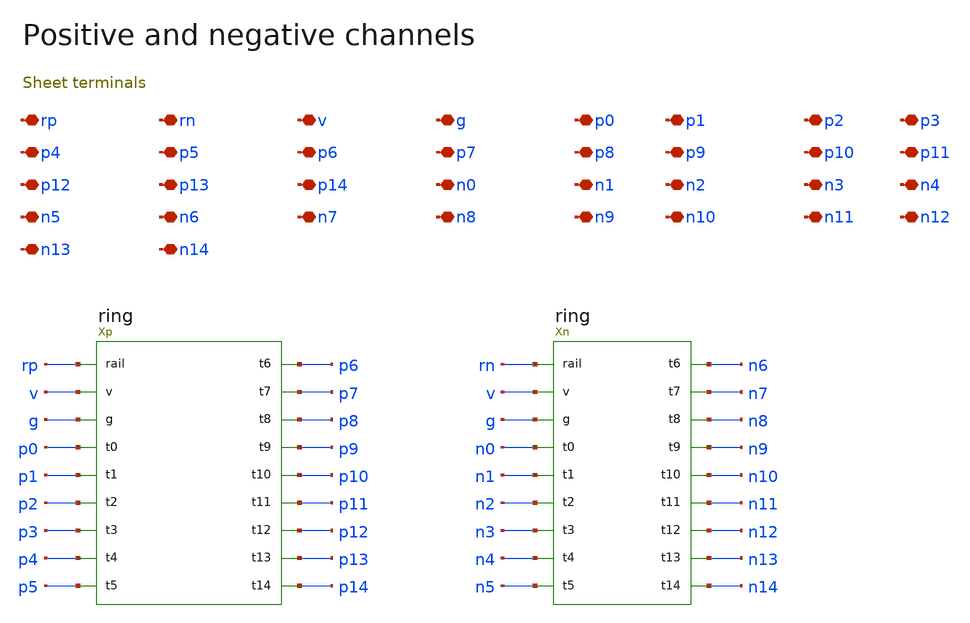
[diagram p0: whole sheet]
** sch_path: review/xschem/dual.sch
**.subckt dual rp rn v g p0 p1 p2 p3 p4 p5 p6 p7 p8 p9 p10 p11 p12 p13 p14 n0 n1 n2 n3 n4 n5 n6 n7
*+ n8 n9 n10 n11 n12 n13 n14
*.iopin rp
*.iopin rn
*.iopin v
*.iopin g
*.iopin p0
*.iopin p1
*.iopin p2
*.iopin p3
*.iopin p4
*.iopin p5
*.iopin p6
*.iopin p7
*.iopin p8
*.iopin p9
*.iopin p10
*.iopin p11
*.iopin p12
*.iopin p13
*.iopin p14
*.iopin n0
*.iopin n1
*.iopin n2
*.iopin n3
*.iopin n4
*.iopin n5
*.iopin n6
*.iopin n7
*.iopin n8
*.iopin n9
*.iopin n10
*.iopin n11
*.iopin n12
*.iopin n13
*.iopin n14
Xp rp v g p0 p1 p2 p3 p4 p5 p6 p7 p8 p9 p10 p11 p12 p13 p14 ring
Xn rn v g n0 n1 n2 n3 n4 n5 n6 n7 n8 n9 n10 n11 n12 n13 n14 ring
**.ends

* expanding   symbol:  ring.sym # of pins=18
** sym_path: review/xschem/ring.sym
** sch_path: review/xschem/ring.sch
.subckt ring rail v g t0 t1 t2 t3 t4 t5 t6 t7 t8 t9 t10 t11 t12 t13 t14
*.iopin rail
*.iopin v
*.iopin g
*.iopin t0
*.iopin t1
*.iopin t2
*.iopin t3
*.iopin t4
*.iopin t5
*.iopin t6
*.iopin t7
*.iopin t8
*.iopin t9
*.iopin t10
*.iopin t11
*.iopin t12
*.iopin t13
*.iopin t14
Xbank rail v g oa0 ob0 oa1 ob1 oa2 ob2 oa3 ob3 oa4 ob4 oa5 ob5 oa6 ob6 oa7 ob7 oa8 ob8 oa9 ob9 oa10
+ ob10 oa11 ob11 oa12 ob12 oa13 ob13 oa14 ob14 bank
Xl0 oa0 ob0 t0 v g cvsl
Xl1 oa1 ob1 t1 v g cvsl
Xl2 oa2 ob2 t2 v g cvsl
Xl3 oa3 ob3 t3 v g cvsl
Xl4 oa4 ob4 t4 v g cvsl
Xl5 oa5 ob5 t5 v g cvsl
Xl6 oa6 ob6 t6 v g cvsl
Xl7 oa7 ob7 t7 v g cvsl
Xl8 oa8 ob8 t8 v g cvsl
Xl9 oa9 ob9 t9 v g cvsl
Xl10 oa10 ob10 t10 v g cvsl
Xl11 oa11 ob11 t11 v g cvsl
Xl12 oa12 ob12 t12 v g cvsl
Xl13 oa13 ob13 t13 v g cvsl
Xl14 oa14 ob14 t14 v g cvsl
.ends


* expanding   symbol:  bank.sym # of pins=33
** sym_path: review/xschem/bank.sym
** sch_path: review/xschem/bank.sch
.subckt bank rail well g oa0 ob0 oa1 ob1 oa2 ob2 oa3 ob3 oa4 ob4 oa5 ob5 oa6 ob6 oa7 ob7 oa8 ob8 oa9
+ ob9 oa10 ob10 oa11 ob11 oa12 ob12 oa13 ob13 oa14 ob14
*.iopin rail
*.iopin well
*.iopin g
*.iopin oa0
*.iopin ob0
*.iopin oa1
*.iopin ob1
*.iopin oa2
*.iopin ob2
*.iopin oa3
*.iopin ob3
*.iopin oa4
*.iopin ob4
*.iopin oa5
*.iopin ob5
*.iopin oa6
*.iopin ob6
*.iopin oa7
*.iopin ob7
*.iopin oa8
*.iopin ob8
*.iopin oa9
*.iopin ob9
*.iopin oa10
*.iopin ob10
*.iopin oa11
*.iopin ob11
*.iopin oa12
*.iopin ob12
*.iopin oa13
*.iopin ob13
*.iopin oa14
*.iopin ob14
X0 oa14 ob14 oa0 ob0 rail g well stage
X1 oa0 ob0 oa1 ob1 rail g well stage
X2 oa1 ob1 oa2 ob2 rail g well stage
X3 oa2 ob2 oa3 ob3 rail g well stage
X4 oa3 ob3 oa4 ob4 rail g well stage
X5 oa4 ob4 oa5 ob5 rail g well stage
X6 oa5 ob5 oa6 ob6 rail g well stage
X7 oa6 ob6 oa7 ob7 rail g well stage
X8 oa7 ob7 oa8 ob8 rail g well stage
X9 oa8 ob8 oa9 ob9 rail g well stage
X10 oa9 ob9 oa10 ob10 rail g well stage
X11 oa10 ob10 oa11 ob11 rail g well stage
X12 oa11 ob11 oa12 ob12 rail g well stage
X13 oa12 ob12 oa13 ob13 rail g well stage
X14 oa13 ob13 oa14 ob14 rail g well stage
Xdummy well well dy dz g g well stage
.ends


* expanding   symbol:  cvsl.sym # of pins=5
** sym_path: review/xschem/cvsl.sym
** sch_path: review/xschem/cvsl.sch
.subckt cvsl a b out v g
*.iopin a
*.iopin b
*.iopin out
*.iopin v
*.iopin g
XMn0 l a g g sky130_fd_pr__nfet_01v8_lvt L=.15 W=4 nf=1 ad=1.16 as=1.16 pd=8.58 ps=8.58 nrd='0.29 / 4 '
+ nrs='0.29 / 4 ' sa=0 sb=0 sd=0 mult=1 m=1
XMn1 r b g g sky130_fd_pr__nfet_01v8_lvt L=.15 W=4 nf=1 ad=1.16 as=1.16 pd=8.58 ps=8.58 nrd='0.29 / 4 '
+ nrs='0.29 / 4 ' sa=0 sb=0 sd=0 mult=1 m=1
XMp0 l r v v sky130_fd_pr__pfet_01v8 L=2.4 W=.42 nf=1 ad=.122 as=.122 pd=1.42 ps=1.42 nrd='0.29 / W'
+ nrs='0.29 / W' sa=0 sb=0 sd=0 mult=1 m=1
XMp1 r l v v sky130_fd_pr__pfet_01v8 L=2.4 W=.42 nf=1 ad=.122 as=.122 pd=1.42 ps=1.42 nrd='0.29 / W'
+ nrs='0.29 / W' sa=0 sb=0 sd=0 mult=1 m=1
XMbuf_p out l v v sky130_fd_pr__pfet_01v8 L=.15 W=.84 nf=1 ad='int((nf+1)/2) * W/nf * 0.29' as='int((nf+2)/2) * W/nf * 0.29'
+ pd='2*int((nf+1)/2) * (W/nf + 0.29)' ps='2*int((nf+2)/2) * (W/nf + 0.29)' nrd='0.29 / W' nrs='0.29 / W'
+ sa=0 sb=0 sd=0 mult=1 m=1
XMbuf_n out l g g sky130_fd_pr__nfet_01v8 L=.15 W=.42 nf=1 ad='int((1 + 1)/2) * .42 / 1 * 0.29' as='int((1 + 2)/2) * .42 / 1 * 0.29'
+ pd='2*int((1 + 1)/2) * (.42 / 1 + 0.29)' ps='2*int((1 + 2)/2) * (.42 / 1 + 0.29)' nrd='0.29 / .42 ' nrs='0.29 / .42 '
+ sa=0 sb=0 sd=0 mult=1 m=1
XMdummy_p dummy r v v sky130_fd_pr__pfet_01v8 L=.15 W=.84 nf=1 ad='int((nf+1)/2) * W/nf * 0.29' as='int((nf+2)/2) * W/nf * 0.29'
+ pd='2*int((nf+1)/2) * (W/nf + 0.29)' ps='2*int((nf+2)/2) * (W/nf + 0.29)' nrd='0.29 / W' nrs='0.29 / W'
+ sa=0 sb=0 sd=0 mult=1 m=1
XMdummy_n dummy r g g sky130_fd_pr__nfet_01v8 L=.15 W=.42 nf=1 ad='int((1 + 1)/2) * .42 / 1 * 0.29' as='int((1 + 2)/2) * .42 / 1 * 0.29'
+ pd='2*int((1 + 1)/2) * (.42 / 1 + 0.29)' ps='2*int((1 + 2)/2) * (.42 / 1 + 0.29)' nrd='0.29 / .42 ' nrs='0.29 / .42 '
+ sa=0 sb=0 sd=0 mult=1 m=1
.ends


* expanding   symbol:  stage.sym # of pins=7
** sym_path: review/xschem/stage.sym
** sch_path: review/xschem/stage.sch
.subckt stage a b y z rail g well
*.iopin a
*.iopin b
*.iopin y
*.iopin z
*.iopin rail
*.iopin g
*.iopin well
XCca g y sky130_fd_pr__cap_mim_m3_1 W=4.5 L=4.5 MF=1 m=1
XCcb g z sky130_fd_pr__cap_mim_m3_1 W=4.5 L=4.5 MF=1 m=1
XMmainA_Xp y a rail well sky130_fd_pr__pfet_01v8_lvt L=.55 W=8.4 nf=1 ad='int((1 + 1)/2) * 8.4 / 1 * 0.29'
+ as='int((1 + 2)/2) * 8.4 / 1 * 0.29' pd='2*int((1 + 1)/2) * (8.4 / 1 + 0.29)' ps='2*int((1 + 2)/2) * (8.4 / 1 + 0.29)'
+ nrd='0.29 / 8.4 ' nrs='0.29 / 8.4 ' sa=0 sb=0 sd=0 mult=1 m=1
XMmainA_Xn y a g g sky130_fd_pr__nfet_01v8 L=.55 W=4.2 nf=1 ad='int((1 + 1)/2) * 4.2 / 1 * 0.29' as='int((1 + 2)/2) * 4.2 / 1 * 0.29'
+ pd='2*int((1 + 1)/2) * (4.2 / 1 + 0.29)' ps='2*int((1 + 2)/2) * (4.2 / 1 + 0.29)' nrd='0.29 / 4.2 ' nrs='0.29 / 4.2 '
+ sa=0 sb=0 sd=0 mult=1 m=1
XMmainB_Xp z b rail well sky130_fd_pr__pfet_01v8_lvt L=.55 W=8.4 nf=1 ad='int((1 + 1)/2) * 8.4 / 1 * 0.29'
+ as='int((1 + 2)/2) * 8.4 / 1 * 0.29' pd='2*int((1 + 1)/2) * (8.4 / 1 + 0.29)' ps='2*int((1 + 2)/2) * (8.4 / 1 + 0.29)'
+ nrd='0.29 / 8.4 ' nrs='0.29 / 8.4 ' sa=0 sb=0 sd=0 mult=1 m=1
XMmainB_Xn z b g g sky130_fd_pr__nfet_01v8 L=.55 W=4.2 nf=1 ad='int((1 + 1)/2) * 4.2 / 1 * 0.29' as='int((1 + 2)/2) * 4.2 / 1 * 0.29'
+ pd='2*int((1 + 1)/2) * (4.2 / 1 + 0.29)' ps='2*int((1 + 2)/2) * (4.2 / 1 + 0.29)' nrd='0.29 / 4.2 ' nrs='0.29 / 4.2 '
+ sa=0 sb=0 sd=0 mult=1 m=1
XMcrossA_Xp z y rail well sky130_fd_pr__pfet_01v8_lvt L=.55 W=1.68 nf=1 ad='int((1 + 1)/2) * 1.68 / 1 * 0.29'
+ as='int((1 + 2)/2) * 1.68 / 1 * 0.29' pd='2*int((1 + 1)/2) * (1.68 / 1 + 0.29)' ps='2*int((1 + 2)/2) * (1.68 / 1 + 0.29)'
+ nrd='0.29 / 1.68 ' nrs='0.29 / 1.68 ' sa=0 sb=0 sd=0 mult=1 m=1
XMcrossA_Xn z y g g sky130_fd_pr__nfet_01v8 L=.55 W=.84 nf=1 ad='int((1 + 1)/2) * .84 / 1 * 0.29' as='int((1 + 2)/2) * .84 / 1 * 0.29'
+ pd='2*int((1 + 1)/2) * (.84 / 1 + 0.29)' ps='2*int((1 + 2)/2) * (.84 / 1 + 0.29)' nrd='0.29 / .84 ' nrs='0.29 / .84 '
+ sa=0 sb=0 sd=0 mult=1 m=1
XMcrossB_Xp y z rail well sky130_fd_pr__pfet_01v8_lvt L=.55 W=1.68 nf=1 ad='int((1 + 1)/2) * 1.68 / 1 * 0.29'
+ as='int((1 + 2)/2) * 1.68 / 1 * 0.29' pd='2*int((1 + 1)/2) * (1.68 / 1 + 0.29)' ps='2*int((1 + 2)/2) * (1.68 / 1 + 0.29)'
+ nrd='0.29 / 1.68 ' nrs='0.29 / 1.68 ' sa=0 sb=0 sd=0 mult=1 m=1
XMcrossB_Xn y z g g sky130_fd_pr__nfet_01v8 L=.55 W=.84 nf=1 ad='int((1 + 1)/2) * .84 / 1 * 0.29' as='int((1 + 2)/2) * .84 / 1 * 0.29'
+ pd='2*int((1 + 1)/2) * (.84 / 1 + 0.29)' ps='2*int((1 + 2)/2) * (.84 / 1 + 0.29)' nrd='0.29 / .84 ' nrs='0.29 / .84 '
+ sa=0 sb=0 sd=0 mult=1 m=1
.ends

.end
